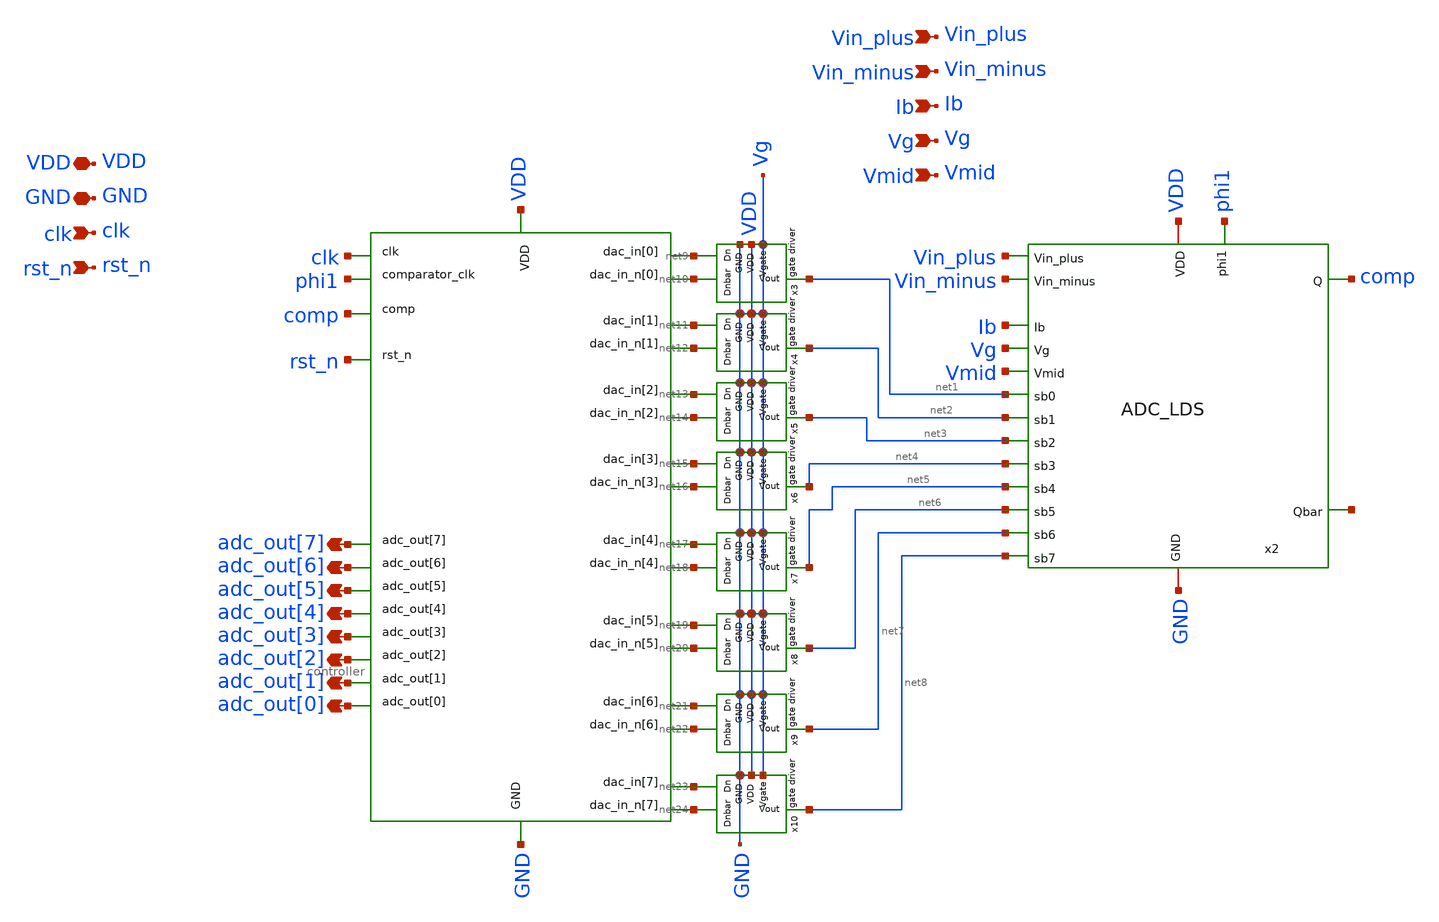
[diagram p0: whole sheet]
** sch_path: final/LDS/adc_final.sch
**.subckt adc_final VDD GND clk rst_n adc_out[0] adc_out[1] adc_out[2] adc_out[3] adc_out[4]
*+ adc_out[5] adc_out[6] adc_out[7] Vin_plus Vin_minus Ib Vg Vmid
*.iopin VDD
*.iopin GND
*.ipin clk
*.ipin rst_n
*.opin adc_out[0]
*.opin adc_out[1]
*.opin adc_out[2]
*.opin adc_out[3]
*.opin adc_out[4]
*.opin adc_out[5]
*.opin adc_out[6]
*.opin adc_out[7]
*.ipin Vin_plus
*.ipin Vin_minus
*.ipin Ib
*.ipin Vg
*.ipin Vmid
x1 GND VDD adc_out[0] adc_out[1] adc_out[2] adc_out[3] adc_out[4] adc_out[5] adc_out[6] adc_out[7]
+ clk comp phi1 net9 net10 net11 net12 net13 net14 net15 net16 net17 net18 net19 net20 net21 net22 net23
+ net24 rst_n controller
x2 Vin_plus Vin_minus Vg Vmid phi1 VDD GND comp net25 net8 Ib net7 net6 net5 net4 net3 net2 net1
+ ADC_LDS
x3 Vg net9 net1 net10 GND VDD gate_driver_LDS
x4 Vg net11 net2 net12 GND VDD gate_driver_LDS
x5 Vg net13 net3 net14 GND VDD gate_driver_LDS
x6 Vg net15 net4 net16 GND VDD gate_driver_LDS
x7 Vg net17 net5 net18 GND VDD gate_driver_LDS
x8 Vg net19 net6 net20 GND VDD gate_driver_LDS
x9 Vg net21 net7 net22 GND VDD gate_driver_LDS
x10 Vg net23 net8 net24 GND VDD gate_driver_LDS
**.ends
.end
